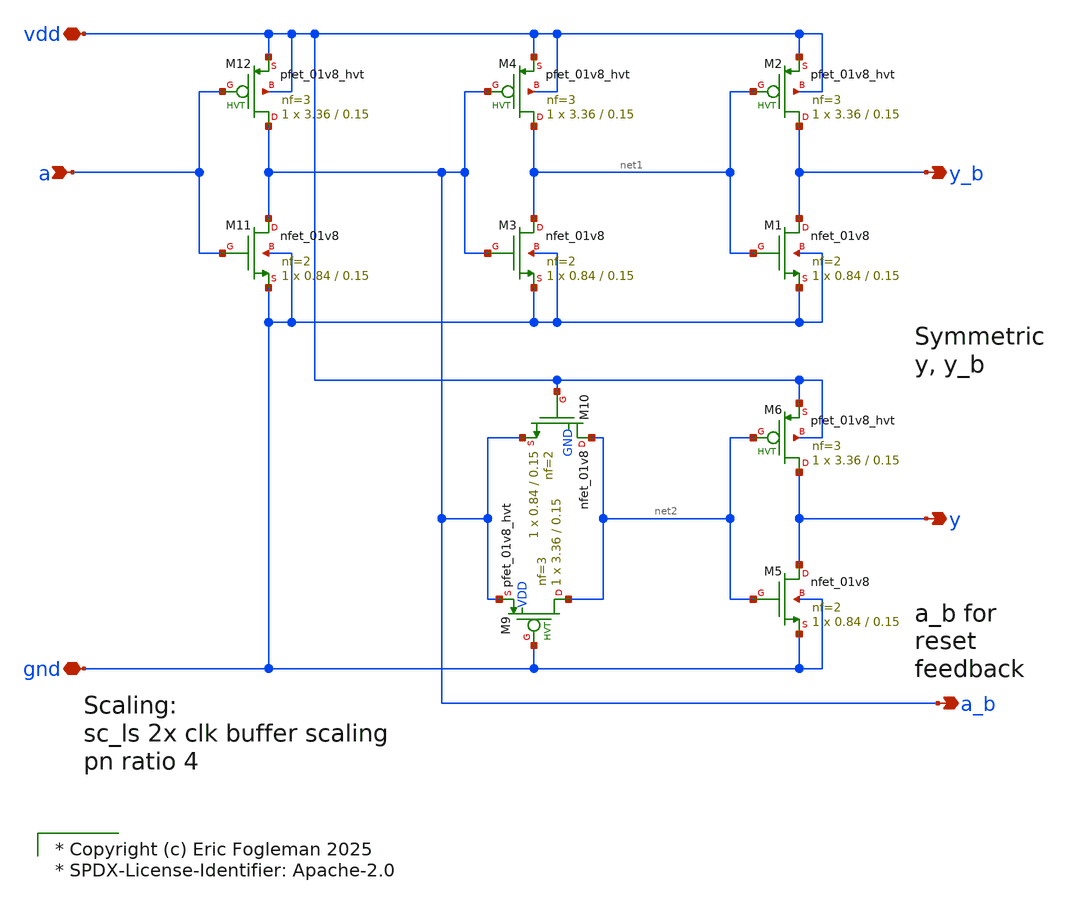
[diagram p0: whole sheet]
** sch_path: xschem/ejf_pll96_diff_buf.sch

* Copyright (c) Eric Fogleman 2025
* SPDX-License-Identifier: Apache-2.0

**.subckt ejf_pll96_diff_buf vdd gnd a y_b y a_b
*.iopin vdd
*.iopin gnd
*.ipin a
*.opin y_b
*.opin y
*.opin a_b
XM11 a_b a gnd gnd sky130_fd_pr__nfet_01v8 L=0.15 W=0.84 nf=2 ad='int((nf+1)/2) * W/nf * 0.29' as='int((nf+2)/2) * W/nf * 0.29'
+ pd='2*int((nf+1)/2) * (W/nf + 0.29)' ps='2*int((nf+2)/2) * (W/nf + 0.29)' nrd='0.29 / W' nrs='0.29 / W'
+ sa=0 sb=0 sd=0 mult=1 m=1
XM12 a_b a vdd vdd sky130_fd_pr__pfet_01v8_hvt L=0.15 W=3.36 nf=3 ad='int((nf+1)/2) * W/nf * 0.29' as='int((nf+2)/2) * W/nf * 0.29'
+ pd='2*int((nf+1)/2) * (W/nf + 0.29)' ps='2*int((nf+2)/2) * (W/nf + 0.29)' nrd='0.29 / W' nrs='0.29 / W'
+ sa=0 sb=0 sd=0 mult=1 m=1
XM1 y_b net1 gnd gnd sky130_fd_pr__nfet_01v8 L=0.15 W=0.84 nf=2 ad='int((nf+1)/2) * W/nf * 0.29' as='int((nf+2)/2) * W/nf * 0.29'
+ pd='2*int((nf+1)/2) * (W/nf + 0.29)' ps='2*int((nf+2)/2) * (W/nf + 0.29)' nrd='0.29 / W' nrs='0.29 / W'
+ sa=0 sb=0 sd=0 mult=1 m=1
XM2 y_b net1 vdd vdd sky130_fd_pr__pfet_01v8_hvt L=0.15 W=3.36 nf=3 ad='int((nf+1)/2) * W/nf * 0.29'
+ as='int((nf+2)/2) * W/nf * 0.29' pd='2*int((nf+1)/2) * (W/nf + 0.29)' ps='2*int((nf+2)/2) * (W/nf + 0.29)'
+ nrd='0.29 / W' nrs='0.29 / W' sa=0 sb=0 sd=0 mult=1 m=1
XM3 net1 a_b gnd gnd sky130_fd_pr__nfet_01v8 L=0.15 W=0.84 nf=2 ad='int((nf+1)/2) * W/nf * 0.29' as='int((nf+2)/2) * W/nf * 0.29'
+ pd='2*int((nf+1)/2) * (W/nf + 0.29)' ps='2*int((nf+2)/2) * (W/nf + 0.29)' nrd='0.29 / W' nrs='0.29 / W'
+ sa=0 sb=0 sd=0 mult=1 m=1
XM4 net1 a_b vdd vdd sky130_fd_pr__pfet_01v8_hvt L=0.15 W=3.36 nf=3 ad='int((nf+1)/2) * W/nf * 0.29'
+ as='int((nf+2)/2) * W/nf * 0.29' pd='2*int((nf+1)/2) * (W/nf + 0.29)' ps='2*int((nf+2)/2) * (W/nf + 0.29)'
+ nrd='0.29 / W' nrs='0.29 / W' sa=0 sb=0 sd=0 mult=1 m=1
XM5 y net2 gnd gnd sky130_fd_pr__nfet_01v8 L=0.15 W=0.84 nf=2 ad='int((nf+1)/2) * W/nf * 0.29' as='int((nf+2)/2) * W/nf * 0.29'
+ pd='2*int((nf+1)/2) * (W/nf + 0.29)' ps='2*int((nf+2)/2) * (W/nf + 0.29)' nrd='0.29 / W' nrs='0.29 / W'
+ sa=0 sb=0 sd=0 mult=1 m=1
XM6 y net2 vdd vdd sky130_fd_pr__pfet_01v8_hvt L=0.15 W=3.36 nf=3 ad='int((nf+1)/2) * W/nf * 0.29' as='int((nf+2)/2) * W/nf * 0.29'
+ pd='2*int((nf+1)/2) * (W/nf + 0.29)' ps='2*int((nf+2)/2) * (W/nf + 0.29)' nrd='0.29 / W' nrs='0.29 / W'
+ sa=0 sb=0 sd=0 mult=1 m=1
XM9 net2 gnd a_b VDD sky130_fd_pr__pfet_01v8_hvt L=0.15 W=3.36 nf=3 ad='int((nf+1)/2) * W/nf * 0.29'
+ as='int((nf+2)/2) * W/nf * 0.29' pd='2*int((nf+1)/2) * (W/nf + 0.29)' ps='2*int((nf+2)/2) * (W/nf + 0.29)'
+ nrd='0.29 / W' nrs='0.29 / W' sa=0 sb=0 sd=0 mult=1 m=1
XM10 net2 vdd a_b GND sky130_fd_pr__nfet_01v8 L=0.15 W=0.84 nf=2 ad='int((nf+1)/2) * W/nf * 0.29' as='int((nf+2)/2) * W/nf * 0.29'
+ pd='2*int((nf+1)/2) * (W/nf + 0.29)' ps='2*int((nf+2)/2) * (W/nf + 0.29)' nrd='0.29 / W' nrs='0.29 / W'
+ sa=0 sb=0 sd=0 mult=1 m=1
**.ends
.end
